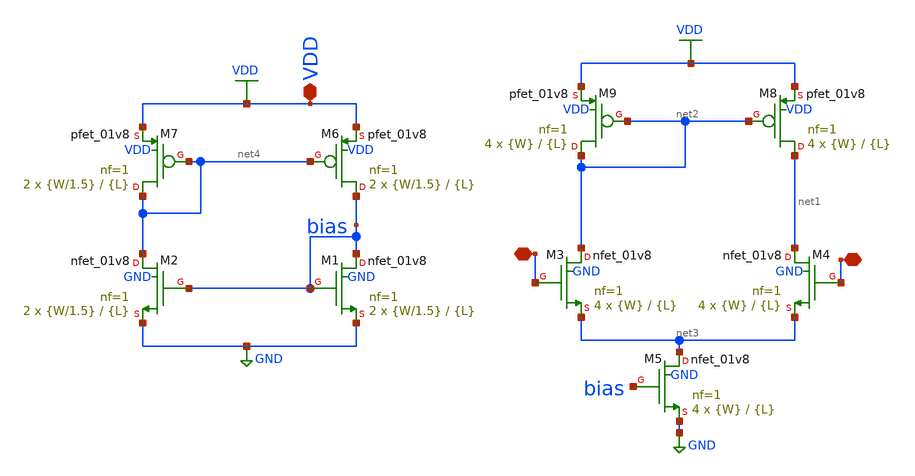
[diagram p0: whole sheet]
** sch_path: xschem/ssa.sch
**.subckt ssa - + VDD
*.iopin -
*.iopin +
*.iopin VDD
XM3 net2 - net3 GND sky130_fd_pr__nfet_01v8 L={L} W={W} nf=1 ad='int((nf+1)/2) * W/nf * 0.29' as='int((nf+2)/2) * W/nf * 0.29'
+ pd='2*int((nf+1)/2) * (W/nf + 0.29)' ps='2*int((nf+2)/2) * (W/nf + 0.29)' nrd='0.29 / W' nrs='0.29 / W'
+ sa=0 sb=0 sd=0 mult=4 m=4
XM4 net1 + net3 GND sky130_fd_pr__nfet_01v8 L={L} W={W} nf=1 ad='int((nf+1)/2) * W/nf * 0.29' as='int((nf+2)/2) * W/nf * 0.29'
+ pd='2*int((nf+1)/2) * (W/nf + 0.29)' ps='2*int((nf+2)/2) * (W/nf + 0.29)' nrd='0.29 / W' nrs='0.29 / W'
+ sa=0 sb=0 sd=0 mult=4 m=4
XM8 net1 net2 VDD VDD sky130_fd_pr__pfet_01v8 L={L} W={W} nf=1 ad='int((nf+1)/2) * W/nf * 0.29' as='int((nf+2)/2) * W/nf * 0.29'
+ pd='2*int((nf+1)/2) * (W/nf + 0.29)' ps='2*int((nf+2)/2) * (W/nf + 0.29)' nrd='0.29 / W' nrs='0.29 / W'
+ sa=0 sb=0 sd=0 mult=4 m=4
XM9 net2 net2 VDD VDD sky130_fd_pr__pfet_01v8 L={L} W={W} nf=1 ad='int((nf+1)/2) * W/nf * 0.29' as='int((nf+2)/2) * W/nf * 0.29'
+ pd='2*int((nf+1)/2) * (W/nf + 0.29)' ps='2*int((nf+2)/2) * (W/nf + 0.29)' nrd='0.29 / W' nrs='0.29 / W'
+ sa=0 sb=0 sd=0 mult=4 m=4
XM5 net3 bias GND GND sky130_fd_pr__nfet_01v8 L={L} W={W} nf=1 ad='int((nf+1)/2) * W/nf * 0.29' as='int((nf+2)/2) * W/nf * 0.29'
+ pd='2*int((nf+1)/2) * (W/nf + 0.29)' ps='2*int((nf+2)/2) * (W/nf + 0.29)' nrd='0.29 / W' nrs='0.29 / W'
+ sa=0 sb=0 sd=0 mult=4 m=4
XM1 bias bias GND GND sky130_fd_pr__nfet_01v8 L={L} W={W/1.5} nf=1 ad='int((nf+1)/2) * W/nf * 0.29' as='int((nf+2)/2) * W/nf * 0.29'
+ pd='2*int((nf+1)/2) * (W/nf + 0.29)' ps='2*int((nf+2)/2) * (W/nf + 0.29)' nrd='0.29 / W' nrs='0.29 / W'
+ sa=0 sb=0 sd=0 mult=2 m=2
XM2 net4 bias GND GND sky130_fd_pr__nfet_01v8 L={L} W={W/1.5} nf=1 ad='int((nf+1)/2) * W/nf * 0.29' as='int((nf+2)/2) * W/nf * 0.29'
+ pd='2*int((nf+1)/2) * (W/nf + 0.29)' ps='2*int((nf+2)/2) * (W/nf + 0.29)' nrd='0.29 / W' nrs='0.29 / W'
+ sa=0 sb=0 sd=0 mult=2 m=2
XM6 bias net4 VDD VDD sky130_fd_pr__pfet_01v8 L={L} W={W/1.5} nf=1 ad='int((nf+1)/2) * W/nf * 0.29' as='int((nf+2)/2) * W/nf * 0.29'
+ pd='2*int((nf+1)/2) * (W/nf + 0.29)' ps='2*int((nf+2)/2) * (W/nf + 0.29)' nrd='0.29 / W' nrs='0.29 / W'
+ sa=0 sb=0 sd=0 mult=2 m=2
XM7 net4 net4 VDD VDD sky130_fd_pr__pfet_01v8 L={L} W={W/1.5} nf=1 ad='int((nf+1)/2) * W/nf * 0.29' as='int((nf+2)/2) * W/nf * 0.29'
+ pd='2*int((nf+1)/2) * (W/nf + 0.29)' ps='2*int((nf+2)/2) * (W/nf + 0.29)' nrd='0.29 / W' nrs='0.29 / W'
+ sa=0 sb=0 sd=0 mult=2 m=2
**** begin user architecture code


.param L=20
.param W=1


**** end user architecture code
**.ends
.GLOBAL VDD
.GLOBAL GND
.end
